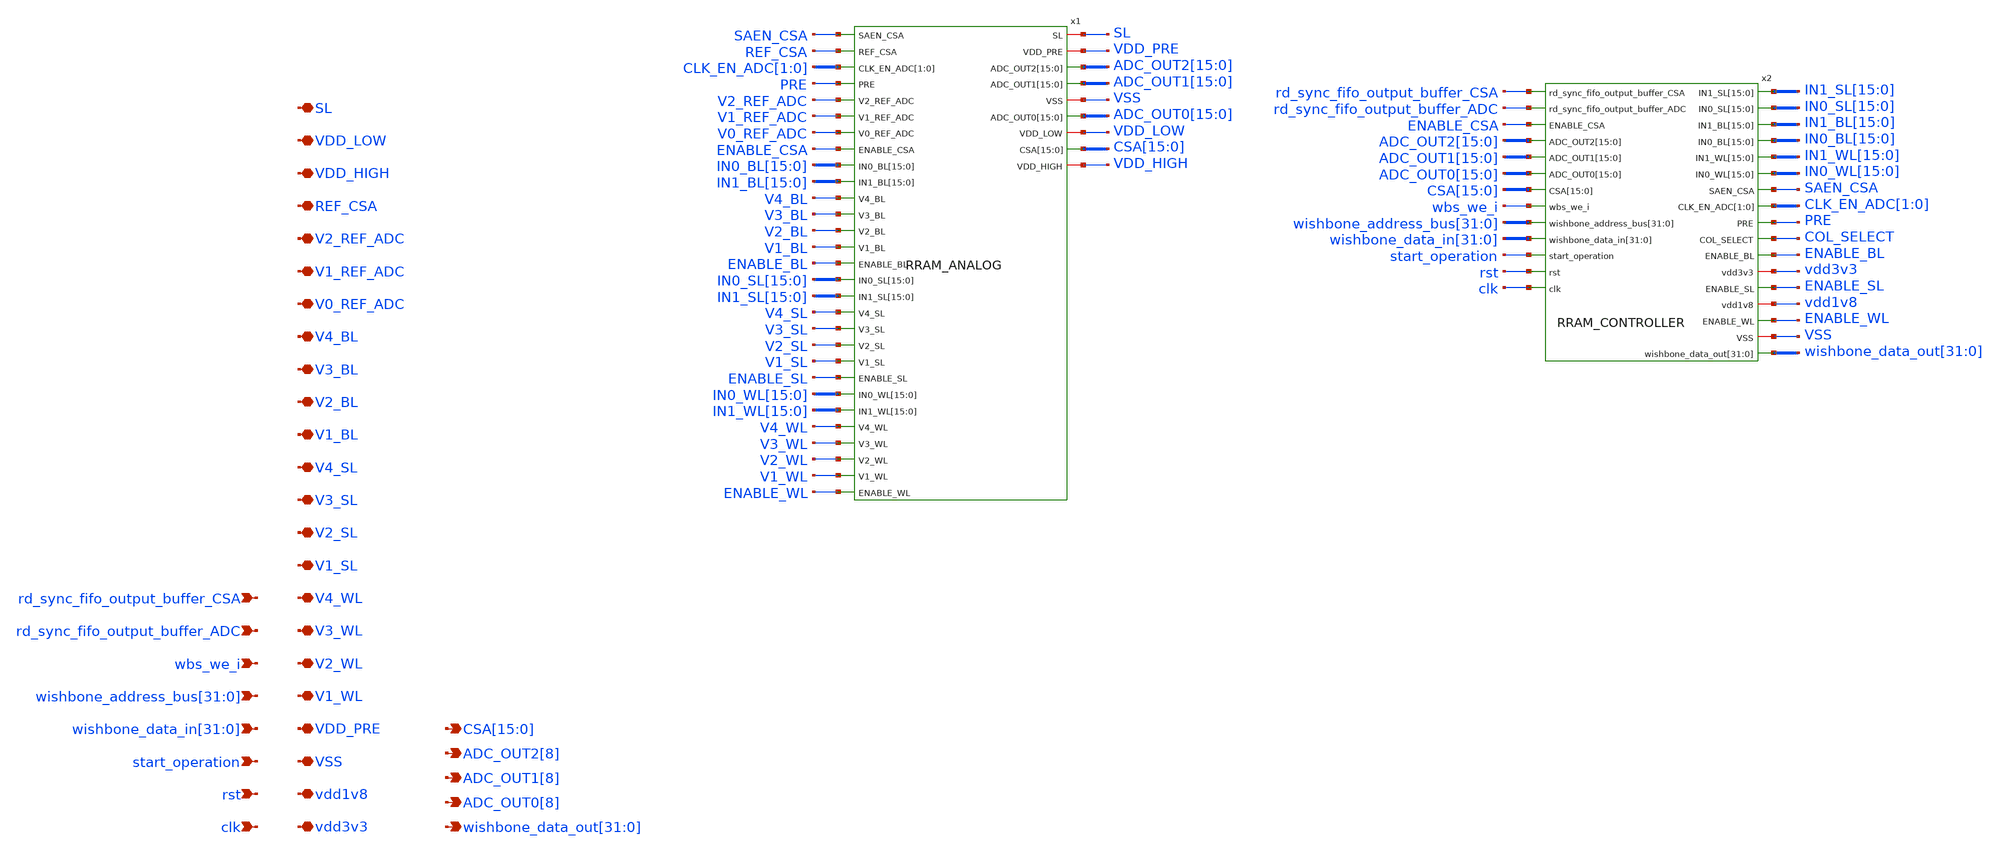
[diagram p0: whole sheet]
** sch_path: xschem/top_wrapper.sch
**.subckt top_wrapper clk rst vdd3v3
*+ wishbone_data_out[31],wishbone_data_out[30],wishbone_data_out[29],wishbone_data_out[28],wishbone_data_out[27],wishbone_data_out[26],wishbone_data_out[25],wishbone_data_out[24],wishbone_data_out[23],wishbone_data_out[22],wishbone_data_out[21],wishbone_data_out[20],wishbone_data_out[19],wishbone_data_out[18],wishbone_data_out[17],wishbone_data_out[16],wishbone_data_out[15],wishbone_data_out[14],wishbone_data_out[13],wishbone_data_out[12],wishbone_data_out[11],wishbone_data_out[10],wishbone_data_out[9],wishbone_data_out[8],wishbone_data_out[7],wishbone_data_out[6],wishbone_data_out[5],wishbone_data_out[4],wishbone_data_out[3],wishbone_data_out[2],wishbone_data_out[1],wishbone_data_out[0] ADC_OUT0[8] vdd1v8 start_operation
*+ wishbone_data_in[31],wishbone_data_in[30],wishbone_data_in[29],wishbone_data_in[28],wishbone_data_in[27],wishbone_data_in[26],wishbone_data_in[25],wishbone_data_in[24],wishbone_data_in[23],wishbone_data_in[22],wishbone_data_in[21],wishbone_data_in[20],wishbone_data_in[19],wishbone_data_in[18],wishbone_data_in[17],wishbone_data_in[16],wishbone_data_in[15],wishbone_data_in[14],wishbone_data_in[13],wishbone_data_in[12],wishbone_data_in[11],wishbone_data_in[10],wishbone_data_in[9],wishbone_data_in[8],wishbone_data_in[7],wishbone_data_in[6],wishbone_data_in[5],wishbone_data_in[4],wishbone_data_in[3],wishbone_data_in[2],wishbone_data_in[1],wishbone_data_in[0]
*+ wishbone_address_bus[31],wishbone_address_bus[30],wishbone_address_bus[29],wishbone_address_bus[28],wishbone_address_bus[27],wishbone_address_bus[26],wishbone_address_bus[25],wishbone_address_bus[24],wishbone_address_bus[23],wishbone_address_bus[22],wishbone_address_bus[21],wishbone_address_bus[20],wishbone_address_bus[19],wishbone_address_bus[18],wishbone_address_bus[17],wishbone_address_bus[16],wishbone_address_bus[15],wishbone_address_bus[14],wishbone_address_bus[13],wishbone_address_bus[12],wishbone_address_bus[11],wishbone_address_bus[10],wishbone_address_bus[9],wishbone_address_bus[8],wishbone_address_bus[7],wishbone_address_bus[6],wishbone_address_bus[5],wishbone_address_bus[4],wishbone_address_bus[3],wishbone_address_bus[2],wishbone_address_bus[1],wishbone_address_bus[0] wbs_we_i VSS VDD_PRE V1_WL V2_WL V3_WL V4_WL V1_SL V2_SL V3_SL V4_SL V1_BL V2_BL V3_BL V4_BL
*+ V0_REF_ADC V1_REF_ADC V2_REF_ADC REF_CSA ADC_OUT1[8] ADC_OUT2[8]
*+ CSA[15],CSA[14],CSA[13],CSA[12],CSA[11],CSA[10],CSA[9],CSA[8],CSA[7],CSA[6],CSA[5],CSA[4],CSA[3],CSA[2],CSA[1],CSA[0] rd_sync_fifo_output_buffer_ADC rd_sync_fifo_output_buffer_CSA VDD_HIGH VDD_LOW SL
*.ipin clk
*.ipin rst
*.iopin vdd3v3
*.opin
*+ wishbone_data_out[31],wishbone_data_out[30],wishbone_data_out[29],wishbone_data_out[28],wishbone_data_out[27],wishbone_data_out[26],wishbone_data_out[25],wishbone_data_out[24],wishbone_data_out[23],wishbone_data_out[22],wishbone_data_out[21],wishbone_data_out[20],wishbone_data_out[19],wishbone_data_out[18],wishbone_data_out[17],wishbone_data_out[16],wishbone_data_out[15],wishbone_data_out[14],wishbone_data_out[13],wishbone_data_out[12],wishbone_data_out[11],wishbone_data_out[10],wishbone_data_out[9],wishbone_data_out[8],wishbone_data_out[7],wishbone_data_out[6],wishbone_data_out[5],wishbone_data_out[4],wishbone_data_out[3],wishbone_data_out[2],wishbone_data_out[1],wishbone_data_out[0]
*.opin ADC_OUT0[8]
*.iopin vdd1v8
*.ipin start_operation
*.ipin
*+ wishbone_data_in[31],wishbone_data_in[30],wishbone_data_in[29],wishbone_data_in[28],wishbone_data_in[27],wishbone_data_in[26],wishbone_data_in[25],wishbone_data_in[24],wishbone_data_in[23],wishbone_data_in[22],wishbone_data_in[21],wishbone_data_in[20],wishbone_data_in[19],wishbone_data_in[18],wishbone_data_in[17],wishbone_data_in[16],wishbone_data_in[15],wishbone_data_in[14],wishbone_data_in[13],wishbone_data_in[12],wishbone_data_in[11],wishbone_data_in[10],wishbone_data_in[9],wishbone_data_in[8],wishbone_data_in[7],wishbone_data_in[6],wishbone_data_in[5],wishbone_data_in[4],wishbone_data_in[3],wishbone_data_in[2],wishbone_data_in[1],wishbone_data_in[0]
*.ipin
*+ wishbone_address_bus[31],wishbone_address_bus[30],wishbone_address_bus[29],wishbone_address_bus[28],wishbone_address_bus[27],wishbone_address_bus[26],wishbone_address_bus[25],wishbone_address_bus[24],wishbone_address_bus[23],wishbone_address_bus[22],wishbone_address_bus[21],wishbone_address_bus[20],wishbone_address_bus[19],wishbone_address_bus[18],wishbone_address_bus[17],wishbone_address_bus[16],wishbone_address_bus[15],wishbone_address_bus[14],wishbone_address_bus[13],wishbone_address_bus[12],wishbone_address_bus[11],wishbone_address_bus[10],wishbone_address_bus[9],wishbone_address_bus[8],wishbone_address_bus[7],wishbone_address_bus[6],wishbone_address_bus[5],wishbone_address_bus[4],wishbone_address_bus[3],wishbone_address_bus[2],wishbone_address_bus[1],wishbone_address_bus[0]
*.ipin wbs_we_i
*.iopin VSS
*.iopin VDD_PRE
*.iopin V1_WL
*.iopin V2_WL
*.iopin V3_WL
*.iopin V4_WL
*.iopin V1_SL
*.iopin V2_SL
*.iopin V3_SL
*.iopin V4_SL
*.iopin V1_BL
*.iopin V2_BL
*.iopin V3_BL
*.iopin V4_BL
*.iopin V0_REF_ADC
*.iopin V1_REF_ADC
*.iopin V2_REF_ADC
*.iopin REF_CSA
*.opin ADC_OUT1[8]
*.opin ADC_OUT2[8]
*.opin
*+ CSA[15],CSA[14],CSA[13],CSA[12],CSA[11],CSA[10],CSA[9],CSA[8],CSA[7],CSA[6],CSA[5],CSA[4],CSA[3],CSA[2],CSA[1],CSA[0]
*.ipin rd_sync_fifo_output_buffer_ADC
*.ipin rd_sync_fifo_output_buffer_CSA
*.iopin VDD_HIGH
*.iopin VDD_LOW
*.iopin SL
x1 SAEN_CSA REF_CSA CLK_EN_ADC[1] CLK_EN_ADC[0] PRE V2_REF_ADC V1_REF_ADC V0_REF_ADC ENABLE_CSA
+ IN0_BL[15] IN0_BL[14] IN0_BL[13] IN0_BL[12] IN0_BL[11] IN0_BL[10] IN0_BL[9] IN0_BL[8] IN0_BL[7] IN0_BL[6]
+ IN0_BL[5] IN0_BL[4] IN0_BL[3] IN0_BL[2] IN0_BL[1] IN0_BL[0] IN1_BL[15] IN1_BL[14] IN1_BL[13] IN1_BL[12]
+ IN1_BL[11] IN1_BL[10] IN1_BL[9] IN1_BL[8] IN1_BL[7] IN1_BL[6] IN1_BL[5] IN1_BL[4] IN1_BL[3] IN1_BL[2]
+ IN1_BL[1] IN1_BL[0] V4_BL V3_BL V2_BL V1_BL ENABLE_BL IN0_SL[15] IN0_SL[14] IN0_SL[13] IN0_SL[12] IN0_SL[11]
+ IN0_SL[10] IN0_SL[9] IN0_SL[8] IN0_SL[7] IN0_SL[6] IN0_SL[5] IN0_SL[4] IN0_SL[3] IN0_SL[2] IN0_SL[1] IN0_SL[0]
+ IN1_SL[15] IN1_SL[14] IN1_SL[13] IN1_SL[12] IN1_SL[11] IN1_SL[10] IN1_SL[9] IN1_SL[8] IN1_SL[7] IN1_SL[6]
+ IN1_SL[5] IN1_SL[4] IN1_SL[3] IN1_SL[2] IN1_SL[1] IN1_SL[0] V4_SL V3_SL V2_SL V1_SL ENABLE_SL IN0_WL[15]
+ IN0_WL[14] IN0_WL[13] IN0_WL[12] IN0_WL[11] IN0_WL[10] IN0_WL[9] IN0_WL[8] IN0_WL[7] IN0_WL[6] IN0_WL[5]
+ IN0_WL[4] IN0_WL[3] IN0_WL[2] IN0_WL[1] IN0_WL[0] IN1_WL[15] IN1_WL[14] IN1_WL[13] IN1_WL[12] IN1_WL[11]
+ IN1_WL[10] IN1_WL[9] IN1_WL[8] IN1_WL[7] IN1_WL[6] IN1_WL[5] IN1_WL[4] IN1_WL[3] IN1_WL[2] IN1_WL[1] IN1_WL[0]
+ V4_WL SL V3_WL VDD_PRE ADC_OUT2[15] ADC_OUT2[14] ADC_OUT2[13] ADC_OUT2[12] ADC_OUT2[11] ADC_OUT2[10]
+ ADC_OUT2[9] ADC_OUT2[8] ADC_OUT2[7] ADC_OUT2[6] ADC_OUT2[5] ADC_OUT2[4] ADC_OUT2[3] ADC_OUT2[2] ADC_OUT2[1]
+ ADC_OUT2[0] V2_WL ADC_OUT1[15] ADC_OUT1[14] ADC_OUT1[13] ADC_OUT1[12] ADC_OUT1[11] ADC_OUT1[10] ADC_OUT1[9]
+ ADC_OUT1[8] ADC_OUT1[7] ADC_OUT1[6] ADC_OUT1[5] ADC_OUT1[4] ADC_OUT1[3] ADC_OUT1[2] ADC_OUT1[1] ADC_OUT1[0] VSS
+ V1_WL ADC_OUT0[15] ADC_OUT0[14] ADC_OUT0[13] ADC_OUT0[12] ADC_OUT0[11] ADC_OUT0[10] ADC_OUT0[9]
+ ADC_OUT0[8] ADC_OUT0[7] ADC_OUT0[6] ADC_OUT0[5] ADC_OUT0[4] ADC_OUT0[3] ADC_OUT0[2] ADC_OUT0[1] ADC_OUT0[0]
+ VDD_LOW CSA[15] CSA[14] CSA[13] CSA[12] CSA[11] CSA[10] CSA[9] CSA[8] CSA[7] CSA[6] CSA[5] CSA[4] CSA[3]
+ CSA[2] CSA[1] CSA[0] ENABLE_WL VDD_HIGH RRAM_ANALOG
x2 rd_sync_fifo_output_buffer_CSA rd_sync_fifo_output_buffer_ADC ENABLE_CSA IN1_SL[15] IN1_SL[14]
+ IN1_SL[13] IN1_SL[12] IN1_SL[11] IN1_SL[10] IN1_SL[9] IN1_SL[8] IN1_SL[7] IN1_SL[6] IN1_SL[5] IN1_SL[4]
+ IN1_SL[3] IN1_SL[2] IN1_SL[1] IN1_SL[0] IN0_SL[15] IN0_SL[14] IN0_SL[13] IN0_SL[12] IN0_SL[11] IN0_SL[10]
+ IN0_SL[9] IN0_SL[8] IN0_SL[7] IN0_SL[6] IN0_SL[5] IN0_SL[4] IN0_SL[3] IN0_SL[2] IN0_SL[1] IN0_SL[0]
+ ADC_OUT2[15] ADC_OUT2[14] ADC_OUT2[13] ADC_OUT2[12] ADC_OUT2[11] ADC_OUT2[10] ADC_OUT2[9] ADC_OUT2[8]
+ ADC_OUT2[7] ADC_OUT2[6] ADC_OUT2[5] ADC_OUT2[4] ADC_OUT2[3] ADC_OUT2[2] ADC_OUT2[1] ADC_OUT2[0] IN1_BL[15]
+ IN1_BL[14] IN1_BL[13] IN1_BL[12] IN1_BL[11] IN1_BL[10] IN1_BL[9] IN1_BL[8] IN1_BL[7] IN1_BL[6] IN1_BL[5]
+ IN1_BL[4] IN1_BL[3] IN1_BL[2] IN1_BL[1] IN1_BL[0] ADC_OUT1[15] ADC_OUT1[14] ADC_OUT1[13] ADC_OUT1[12]
+ ADC_OUT1[11] ADC_OUT1[10] ADC_OUT1[9] ADC_OUT1[8] ADC_OUT1[7] ADC_OUT1[6] ADC_OUT1[5] ADC_OUT1[4] ADC_OUT1[3]
+ ADC_OUT1[2] ADC_OUT1[1] ADC_OUT1[0] IN0_BL[15] IN0_BL[14] IN0_BL[13] IN0_BL[12] IN0_BL[11] IN0_BL[10] IN0_BL[9]
+ IN0_BL[8] IN0_BL[7] IN0_BL[6] IN0_BL[5] IN0_BL[4] IN0_BL[3] IN0_BL[2] IN0_BL[1] IN0_BL[0] ADC_OUT0[15]
+ ADC_OUT0[14] ADC_OUT0[13] ADC_OUT0[12] ADC_OUT0[11] ADC_OUT0[10] ADC_OUT0[9] ADC_OUT0[8] ADC_OUT0[7] ADC_OUT0[6]
+ ADC_OUT0[5] ADC_OUT0[4] ADC_OUT0[3] ADC_OUT0[2] ADC_OUT0[1] ADC_OUT0[0] IN1_WL[15] IN1_WL[14] IN1_WL[13]
+ IN1_WL[12] IN1_WL[11] IN1_WL[10] IN1_WL[9] IN1_WL[8] IN1_WL[7] IN1_WL[6] IN1_WL[5] IN1_WL[4] IN1_WL[3]
+ IN1_WL[2] IN1_WL[1] IN1_WL[0] IN0_WL[15] IN0_WL[14] IN0_WL[13] IN0_WL[12] IN0_WL[11] IN0_WL[10] IN0_WL[9]
+ IN0_WL[8] IN0_WL[7] IN0_WL[6] IN0_WL[5] IN0_WL[4] IN0_WL[3] IN0_WL[2] IN0_WL[1] IN0_WL[0] CSA[15] CSA[14]
+ CSA[13] CSA[12] CSA[11] CSA[10] CSA[9] CSA[8] CSA[7] CSA[6] CSA[5] CSA[4] CSA[3] CSA[2] CSA[1] CSA[0]
+ SAEN_CSA wbs_we_i CLK_EN_ADC[1] CLK_EN_ADC[0] wishbone_address_bus[31] wishbone_address_bus[30]
+ wishbone_address_bus[29] wishbone_address_bus[28] wishbone_address_bus[27] wishbone_address_bus[26] wishbone_address_bus[25]
+ wishbone_address_bus[24] wishbone_address_bus[23] wishbone_address_bus[22] wishbone_address_bus[21] wishbone_address_bus[20]
+ wishbone_address_bus[19] wishbone_address_bus[18] wishbone_address_bus[17] wishbone_address_bus[16] wishbone_address_bus[15]
+ wishbone_address_bus[14] wishbone_address_bus[13] wishbone_address_bus[12] wishbone_address_bus[11] wishbone_address_bus[10]
+ wishbone_address_bus[9] wishbone_address_bus[8] wishbone_address_bus[7] wishbone_address_bus[6] wishbone_address_bus[5]
+ wishbone_address_bus[4] wishbone_address_bus[3] wishbone_address_bus[2] wishbone_address_bus[1] wishbone_address_bus[0] PRE
+ wishbone_data_in[31] wishbone_data_in[30] wishbone_data_in[29] wishbone_data_in[28] wishbone_data_in[27]
+ wishbone_data_in[26] wishbone_data_in[25] wishbone_data_in[24] wishbone_data_in[23] wishbone_data_in[22]
+ wishbone_data_in[21] wishbone_data_in[20] wishbone_data_in[19] wishbone_data_in[18] wishbone_data_in[17]
+ wishbone_data_in[16] wishbone_data_in[15] wishbone_data_in[14] wishbone_data_in[13] wishbone_data_in[12]
+ wishbone_data_in[11] wishbone_data_in[10] wishbone_data_in[9] wishbone_data_in[8] wishbone_data_in[7]
+ wishbone_data_in[6] wishbone_data_in[5] wishbone_data_in[4] wishbone_data_in[3] wishbone_data_in[2] wishbone_data_in[1]
+ wishbone_data_in[0] COL_SELECT ENABLE_BL start_operation vdd3v3 ENABLE_SL vdd1v8 rst ENABLE_WL VSS
+ wishbone_data_out[31] wishbone_data_out[30] wishbone_data_out[29] wishbone_data_out[28] wishbone_data_out[27]
+ wishbone_data_out[26] wishbone_data_out[25] wishbone_data_out[24] wishbone_data_out[23] wishbone_data_out[22]
+ wishbone_data_out[21] wishbone_data_out[20] wishbone_data_out[19] wishbone_data_out[18] wishbone_data_out[17]
+ wishbone_data_out[16] wishbone_data_out[15] wishbone_data_out[14] wishbone_data_out[13] wishbone_data_out[12]
+ wishbone_data_out[11] wishbone_data_out[10] wishbone_data_out[9] wishbone_data_out[8] wishbone_data_out[7]
+ wishbone_data_out[6] wishbone_data_out[5] wishbone_data_out[4] wishbone_data_out[3] wishbone_data_out[2]
+ wishbone_data_out[1] wishbone_data_out[0] clk RRAM_CONTROLLER
**.ends

* expanding   symbol:  RRAM_IMC/xschem/RRAM_ANALOG.sym # of pins=38
** sym_path: xschem/RRAM_ANALOG.sym
** sch_path: xschem/RRAM_ANALOG.sch
.subckt RRAM_ANALOG SAEN_CSA REF_CSA CLK_EN_ADC[1] CLK_EN_ADC[0] PRE V2_REF_ADC V1_REF_ADC
+ V0_REF_ADC ENABLE_CSA IN0_BL[15] IN0_BL[14] IN0_BL[13] IN0_BL[12] IN0_BL[11] IN0_BL[10] IN0_BL[9] IN0_BL[8]
+ IN0_BL[7] IN0_BL[6] IN0_BL[5] IN0_BL[4] IN0_BL[3] IN0_BL[2] IN0_BL[1] IN0_BL[0] IN1_BL[15] IN1_BL[14]
+ IN1_BL[13] IN1_BL[12] IN1_BL[11] IN1_BL[10] IN1_BL[9] IN1_BL[8] IN1_BL[7] IN1_BL[6] IN1_BL[5] IN1_BL[4]
+ IN1_BL[3] IN1_BL[2] IN1_BL[1] IN1_BL[0] V4_BL V3_BL V2_BL V1_BL ENABLE_BL IN0_SL[15] IN0_SL[14] IN0_SL[13]
+ IN0_SL[12] IN0_SL[11] IN0_SL[10] IN0_SL[9] IN0_SL[8] IN0_SL[7] IN0_SL[6] IN0_SL[5] IN0_SL[4] IN0_SL[3]
+ IN0_SL[2] IN0_SL[1] IN0_SL[0] IN1_SL[15] IN1_SL[14] IN1_SL[13] IN1_SL[12] IN1_SL[11] IN1_SL[10] IN1_SL[9]
+ IN1_SL[8] IN1_SL[7] IN1_SL[6] IN1_SL[5] IN1_SL[4] IN1_SL[3] IN1_SL[2] IN1_SL[1] IN1_SL[0] V4_SL V3_SL V2_SL
+ V1_SL ENABLE_SL IN0_WL[15] IN0_WL[14] IN0_WL[13] IN0_WL[12] IN0_WL[11] IN0_WL[10] IN0_WL[9] IN0_WL[8]
+ IN0_WL[7] IN0_WL[6] IN0_WL[5] IN0_WL[4] IN0_WL[3] IN0_WL[2] IN0_WL[1] IN0_WL[0] IN1_WL[15] IN1_WL[14]
+ IN1_WL[13] IN1_WL[12] IN1_WL[11] IN1_WL[10] IN1_WL[9] IN1_WL[8] IN1_WL[7] IN1_WL[6] IN1_WL[5] IN1_WL[4]
+ IN1_WL[3] IN1_WL[2] IN1_WL[1] IN1_WL[0] V4_WL SL V3_WL VDD_PRE ADC_OUT2[15] ADC_OUT2[14] ADC_OUT2[13]
+ ADC_OUT2[12] ADC_OUT2[11] ADC_OUT2[10] ADC_OUT2[9] ADC_OUT2[8] ADC_OUT2[7] ADC_OUT2[6] ADC_OUT2[5] ADC_OUT2[4]
+ ADC_OUT2[3] ADC_OUT2[2] ADC_OUT2[1] ADC_OUT2[0] V2_WL ADC_OUT1[15] ADC_OUT1[14] ADC_OUT1[13] ADC_OUT1[12]
+ ADC_OUT1[11] ADC_OUT1[10] ADC_OUT1[9] ADC_OUT1[8] ADC_OUT1[7] ADC_OUT1[6] ADC_OUT1[5] ADC_OUT1[4] ADC_OUT1[3]
+ ADC_OUT1[2] ADC_OUT1[1] ADC_OUT1[0] VSS V1_WL ADC_OUT0[15] ADC_OUT0[14] ADC_OUT0[13] ADC_OUT0[12] ADC_OUT0[11]
+ ADC_OUT0[10] ADC_OUT0[9] ADC_OUT0[8] ADC_OUT0[7] ADC_OUT0[6] ADC_OUT0[5] ADC_OUT0[4] ADC_OUT0[3] ADC_OUT0[2]
+ ADC_OUT0[1] ADC_OUT0[0] VDD_LOW CSA[15] CSA[14] CSA[13] CSA[12] CSA[11] CSA[10] CSA[9] CSA[8] CSA[7] CSA[6]
+ CSA[5] CSA[4] CSA[3] CSA[2] CSA[1] CSA[0] ENABLE_WL VDD_HIGH
*.iopin VDD_HIGH
*.iopin VDD_LOW
*.opin
*+ CSA[15],CSA[14],CSA[13],CSA[12],CSA[11],CSA[10],CSA[9],CSA[8],CSA[7],CSA[6],CSA[5],CSA[4],CSA[3],CSA[2],CSA[1],CSA[0]
*.ipin V1_WL
*.ipin V2_WL
*.ipin V3_WL
*.ipin V4_WL
*.ipin
*+ IN1_WL[15],IN1_WL[14],IN1_WL[13],IN1_WL[12],IN1_WL[11],IN1_WL[10],IN1_WL[9],IN1_WL[8],IN1_WL[7],IN1_WL[6],IN1_WL[5],IN1_WL[4],IN1_WL[3],IN1_WL[2],IN1_WL[1],IN1_WL[0]
*.ipin
*+ IN0_WL[15],IN0_WL[14],IN0_WL[13],IN0_WL[12],IN0_WL[11],IN0_WL[10],IN0_WL[9],IN0_WL[8],IN0_WL[7],IN0_WL[6],IN0_WL[5],IN0_WL[4],IN0_WL[3],IN0_WL[2],IN0_WL[1],IN0_WL[0]
*.ipin ENABLE_SL
*.ipin V1_SL
*.ipin V2_SL
*.ipin V3_SL
*.ipin V4_SL
*.ipin
*+ IN1_SL[15],IN1_SL[14],IN1_SL[13],IN1_SL[12],IN1_SL[11],IN1_SL[10],IN1_SL[9],IN1_SL[8],IN1_SL[7],IN1_SL[6],IN1_SL[5],IN1_SL[4],IN1_SL[3],IN1_SL[2],IN1_SL[1],IN1_SL[0]
*.ipin
*+ IN0_SL[15],IN0_SL[14],IN0_SL[13],IN0_SL[12],IN0_SL[11],IN0_SL[10],IN0_SL[9],IN0_SL[8],IN0_SL[7],IN0_SL[6],IN0_SL[5],IN0_SL[4],IN0_SL[3],IN0_SL[2],IN0_SL[1],IN0_SL[0]
*.ipin ENABLE_BL
*.ipin V1_BL
*.ipin V2_BL
*.ipin V3_BL
*.ipin V4_BL
*.ipin
*+ IN1_BL[15],IN1_BL[14],IN1_BL[13],IN1_BL[12],IN1_BL[11],IN1_BL[10],IN1_BL[9],IN1_BL[8],IN1_BL[7],IN1_BL[6],IN1_BL[5],IN1_BL[4],IN1_BL[3],IN1_BL[2],IN1_BL[1],IN1_BL[0]
*.ipin
*+ IN0_BL[15],IN0_BL[14],IN0_BL[13],IN0_BL[12],IN0_BL[11],IN0_BL[10],IN0_BL[9],IN0_BL[8],IN0_BL[7],IN0_BL[6],IN0_BL[5],IN0_BL[4],IN0_BL[3],IN0_BL[2],IN0_BL[1],IN0_BL[0]
*.ipin ENABLE_CSA
*.ipin V0_REF_ADC
*.ipin V1_REF_ADC
*.ipin V2_REF_ADC
*.ipin PRE
*.iopin VSS
*.opin
*+ ADC_OUT0[15],ADC_OUT0[14],ADC_OUT0[13],ADC_OUT0[12],ADC_OUT0[11],ADC_OUT0[10],ADC_OUT0[9],ADC_OUT0[8],ADC_OUT0[7],ADC_OUT0[6],ADC_OUT0[5],ADC_OUT0[4],ADC_OUT0[3],ADC_OUT0[2],ADC_OUT0[1],ADC_OUT0[0]
*.opin
*+ ADC_OUT1[15],ADC_OUT1[14],ADC_OUT1[13],ADC_OUT1[12],ADC_OUT1[11],ADC_OUT1[10],ADC_OUT1[9],ADC_OUT1[8],ADC_OUT1[7],ADC_OUT1[6],ADC_OUT1[5],ADC_OUT1[4],ADC_OUT1[3],ADC_OUT1[2],ADC_OUT1[1],ADC_OUT1[0]
*.opin
*+ ADC_OUT2[15],ADC_OUT2[14],ADC_OUT2[13],ADC_OUT2[12],ADC_OUT2[11],ADC_OUT2[10],ADC_OUT2[9],ADC_OUT2[8],ADC_OUT2[7],ADC_OUT2[6],ADC_OUT2[5],ADC_OUT2[4],ADC_OUT2[3],ADC_OUT2[2],ADC_OUT2[1],ADC_OUT2[0]
*.ipin CLK_EN_ADC[1],CLK_EN_ADC[0]
*.ipin REF_CSA
*.ipin SAEN_CSA
*.ipin ENABLE_WL
*.iopin VDD_PRE
*.iopin SL
.ends


* expanding   symbol:  RRAM_IMC/xschem/RRAM_CONTROLLER.sym # of pins=30
** sym_path: xschem/RRAM_CONTROLLER.sym
** sch_path: xschem/RRAM_CONTROLLER.sch
.subckt RRAM_CONTROLLER rd_sync_fifo_output_buffer_CSA rd_sync_fifo_output_buffer_ADC ENABLE_CSA
+ IN1_SL[15] IN1_SL[14] IN1_SL[13] IN1_SL[12] IN1_SL[11] IN1_SL[10] IN1_SL[9] IN1_SL[8] IN1_SL[7] IN1_SL[6]
+ IN1_SL[5] IN1_SL[4] IN1_SL[3] IN1_SL[2] IN1_SL[1] IN1_SL[0] IN0_SL[15] IN0_SL[14] IN0_SL[13] IN0_SL[12]
+ IN0_SL[11] IN0_SL[10] IN0_SL[9] IN0_SL[8] IN0_SL[7] IN0_SL[6] IN0_SL[5] IN0_SL[4] IN0_SL[3] IN0_SL[2]
+ IN0_SL[1] IN0_SL[0] ADC_OUT2[15] ADC_OUT2[14] ADC_OUT2[13] ADC_OUT2[12] ADC_OUT2[11] ADC_OUT2[10] ADC_OUT2[9]
+ ADC_OUT2[8] ADC_OUT2[7] ADC_OUT2[6] ADC_OUT2[5] ADC_OUT2[4] ADC_OUT2[3] ADC_OUT2[2] ADC_OUT2[1] ADC_OUT2[0]
+ IN1_BL[15] IN1_BL[14] IN1_BL[13] IN1_BL[12] IN1_BL[11] IN1_BL[10] IN1_BL[9] IN1_BL[8] IN1_BL[7] IN1_BL[6]
+ IN1_BL[5] IN1_BL[4] IN1_BL[3] IN1_BL[2] IN1_BL[1] IN1_BL[0] ADC_OUT1[15] ADC_OUT1[14] ADC_OUT1[13]
+ ADC_OUT1[12] ADC_OUT1[11] ADC_OUT1[10] ADC_OUT1[9] ADC_OUT1[8] ADC_OUT1[7] ADC_OUT1[6] ADC_OUT1[5] ADC_OUT1[4]
+ ADC_OUT1[3] ADC_OUT1[2] ADC_OUT1[1] ADC_OUT1[0] IN0_BL[15] IN0_BL[14] IN0_BL[13] IN0_BL[12] IN0_BL[11]
+ IN0_BL[10] IN0_BL[9] IN0_BL[8] IN0_BL[7] IN0_BL[6] IN0_BL[5] IN0_BL[4] IN0_BL[3] IN0_BL[2] IN0_BL[1] IN0_BL[0]
+ ADC_OUT0[15] ADC_OUT0[14] ADC_OUT0[13] ADC_OUT0[12] ADC_OUT0[11] ADC_OUT0[10] ADC_OUT0[9] ADC_OUT0[8]
+ ADC_OUT0[7] ADC_OUT0[6] ADC_OUT0[5] ADC_OUT0[4] ADC_OUT0[3] ADC_OUT0[2] ADC_OUT0[1] ADC_OUT0[0] IN1_WL[15]
+ IN1_WL[14] IN1_WL[13] IN1_WL[12] IN1_WL[11] IN1_WL[10] IN1_WL[9] IN1_WL[8] IN1_WL[7] IN1_WL[6] IN1_WL[5]
+ IN1_WL[4] IN1_WL[3] IN1_WL[2] IN1_WL[1] IN1_WL[0] IN0_WL[15] IN0_WL[14] IN0_WL[13] IN0_WL[12] IN0_WL[11]
+ IN0_WL[10] IN0_WL[9] IN0_WL[8] IN0_WL[7] IN0_WL[6] IN0_WL[5] IN0_WL[4] IN0_WL[3] IN0_WL[2] IN0_WL[1] IN0_WL[0]
+ CSA[15] CSA[14] CSA[13] CSA[12] CSA[11] CSA[10] CSA[9] CSA[8] CSA[7] CSA[6] CSA[5] CSA[4] CSA[3] CSA[2]
+ CSA[1] CSA[0] SAEN_CSA wbs_we_i CLK_EN_ADC[1] CLK_EN_ADC[0] wishbone_address_bus[31]
+ wishbone_address_bus[30] wishbone_address_bus[29] wishbone_address_bus[28] wishbone_address_bus[27] wishbone_address_bus[26]
+ wishbone_address_bus[25] wishbone_address_bus[24] wishbone_address_bus[23] wishbone_address_bus[22] wishbone_address_bus[21]
+ wishbone_address_bus[20] wishbone_address_bus[19] wishbone_address_bus[18] wishbone_address_bus[17] wishbone_address_bus[16]
+ wishbone_address_bus[15] wishbone_address_bus[14] wishbone_address_bus[13] wishbone_address_bus[12] wishbone_address_bus[11]
+ wishbone_address_bus[10] wishbone_address_bus[9] wishbone_address_bus[8] wishbone_address_bus[7] wishbone_address_bus[6]
+ wishbone_address_bus[5] wishbone_address_bus[4] wishbone_address_bus[3] wishbone_address_bus[2] wishbone_address_bus[1]
+ wishbone_address_bus[0] PRE wishbone_data_in[31] wishbone_data_in[30] wishbone_data_in[29] wishbone_data_in[28]
+ wishbone_data_in[27] wishbone_data_in[26] wishbone_data_in[25] wishbone_data_in[24] wishbone_data_in[23]
+ wishbone_data_in[22] wishbone_data_in[21] wishbone_data_in[20] wishbone_data_in[19] wishbone_data_in[18]
+ wishbone_data_in[17] wishbone_data_in[16] wishbone_data_in[15] wishbone_data_in[14] wishbone_data_in[13]
+ wishbone_data_in[12] wishbone_data_in[11] wishbone_data_in[10] wishbone_data_in[9] wishbone_data_in[8]
+ wishbone_data_in[7] wishbone_data_in[6] wishbone_data_in[5] wishbone_data_in[4] wishbone_data_in[3] wishbone_data_in[2]
+ wishbone_data_in[1] wishbone_data_in[0] COL_SELECT ENABLE_BL start_operation vdd3v3 ENABLE_SL vdd1v8 rst ENABLE_WL VSS
+ wishbone_data_out[31] wishbone_data_out[30] wishbone_data_out[29] wishbone_data_out[28] wishbone_data_out[27]
+ wishbone_data_out[26] wishbone_data_out[25] wishbone_data_out[24] wishbone_data_out[23] wishbone_data_out[22]
+ wishbone_data_out[21] wishbone_data_out[20] wishbone_data_out[19] wishbone_data_out[18] wishbone_data_out[17]
+ wishbone_data_out[16] wishbone_data_out[15] wishbone_data_out[14] wishbone_data_out[13] wishbone_data_out[12]
+ wishbone_data_out[11] wishbone_data_out[10] wishbone_data_out[9] wishbone_data_out[8] wishbone_data_out[7]
+ wishbone_data_out[6] wishbone_data_out[5] wishbone_data_out[4] wishbone_data_out[3] wishbone_data_out[2]
+ wishbone_data_out[1] wishbone_data_out[0] clk
*.ipin clk
*.ipin rst
*.iopin VSS
*.opin
*+ wishbone_data_out[31],wishbone_data_out[30],wishbone_data_out[29],wishbone_data_out[28],wishbone_data_out[27],wishbone_data_out[26],wishbone_data_out[25],wishbone_data_out[24],wishbone_data_out[23],wishbone_data_out[22],wishbone_data_out[21],wishbone_data_out[20],wishbone_data_out[19],wishbone_data_out[18],wishbone_data_out[17],wishbone_data_out[16],wishbone_data_out[15],wishbone_data_out[14],wishbone_data_out[13],wishbone_data_out[12],wishbone_data_out[11],wishbone_data_out[10],wishbone_data_out[9],wishbone_data_out[8],wishbone_data_out[7],wishbone_data_out[6],wishbone_data_out[5],wishbone_data_out[4],wishbone_data_out[3],wishbone_data_out[2],wishbone_data_out[1],wishbone_data_out[0]
*.opin ENABLE_WL
*.ipin start_operation
*.ipin
*+ wishbone_data_in[31],wishbone_data_in[30],wishbone_data_in[29],wishbone_data_in[28],wishbone_data_in[27],wishbone_data_in[26],wishbone_data_in[25],wishbone_data_in[24],wishbone_data_in[23],wishbone_data_in[22],wishbone_data_in[21],wishbone_data_in[20],wishbone_data_in[19],wishbone_data_in[18],wishbone_data_in[17],wishbone_data_in[16],wishbone_data_in[15],wishbone_data_in[14],wishbone_data_in[13],wishbone_data_in[12],wishbone_data_in[11],wishbone_data_in[10],wishbone_data_in[9],wishbone_data_in[8],wishbone_data_in[7],wishbone_data_in[6],wishbone_data_in[5],wishbone_data_in[4],wishbone_data_in[3],wishbone_data_in[2],wishbone_data_in[1],wishbone_data_in[0]
*.ipin
*+ wishbone_address_bus[31],wishbone_address_bus[30],wishbone_address_bus[29],wishbone_address_bus[28],wishbone_address_bus[27],wishbone_address_bus[26],wishbone_address_bus[25],wishbone_address_bus[24],wishbone_address_bus[23],wishbone_address_bus[22],wishbone_address_bus[21],wishbone_address_bus[20],wishbone_address_bus[19],wishbone_address_bus[18],wishbone_address_bus[17],wishbone_address_bus[16],wishbone_address_bus[15],wishbone_address_bus[14],wishbone_address_bus[13],wishbone_address_bus[12],wishbone_address_bus[11],wishbone_address_bus[10],wishbone_address_bus[9],wishbone_address_bus[8],wishbone_address_bus[7],wishbone_address_bus[6],wishbone_address_bus[5],wishbone_address_bus[4],wishbone_address_bus[3],wishbone_address_bus[2],wishbone_address_bus[1],wishbone_address_bus[0]
*.ipin wbs_we_i
*.ipin
*+ CSA[15],CSA[14],CSA[13],CSA[12],CSA[11],CSA[10],CSA[9],CSA[8],CSA[7],CSA[6],CSA[5],CSA[4],CSA[3],CSA[2],CSA[1],CSA[0]
*.ipin
*+ ADC_OUT0[15],ADC_OUT0[14],ADC_OUT0[13],ADC_OUT0[12],ADC_OUT0[11],ADC_OUT0[10],ADC_OUT0[9],ADC_OUT0[8],ADC_OUT0[7],ADC_OUT0[6],ADC_OUT0[5],ADC_OUT0[4],ADC_OUT0[3],ADC_OUT0[2],ADC_OUT0[1],ADC_OUT0[0]
*.ipin
*+ ADC_OUT1[15],ADC_OUT1[14],ADC_OUT1[13],ADC_OUT1[12],ADC_OUT1[11],ADC_OUT1[10],ADC_OUT1[9],ADC_OUT1[8],ADC_OUT1[7],ADC_OUT1[6],ADC_OUT1[5],ADC_OUT1[4],ADC_OUT1[3],ADC_OUT1[2],ADC_OUT1[1],ADC_OUT1[0]
*.ipin
*+ ADC_OUT2[15],ADC_OUT2[14],ADC_OUT2[13],ADC_OUT2[12],ADC_OUT2[11],ADC_OUT2[10],ADC_OUT2[9],ADC_OUT2[8],ADC_OUT2[7],ADC_OUT2[6],ADC_OUT2[5],ADC_OUT2[4],ADC_OUT2[3],ADC_OUT2[2],ADC_OUT2[1],ADC_OUT2[0]
*.ipin ENABLE_CSA
*.ipin rd_sync_fifo_output_buffer_ADC
*.ipin rd_sync_fifo_output_buffer_CSA
*.iopin vdd1v8
*.iopin vdd3v3
*.opin ENABLE_SL
*.opin ENABLE_BL
*.opin COL_SELECT
*.opin PRE
*.opin CLK_EN_ADC[1],CLK_EN_ADC[0]
*.opin SAEN_CSA
*.opin
*+ IN0_WL[15],IN0_WL[14],IN0_WL[13],IN0_WL[12],IN0_WL[11],IN0_WL[10],IN0_WL[9],IN0_WL[8],IN0_WL[7],IN0_WL[6],IN0_WL[5],IN0_WL[4],IN0_WL[3],IN0_WL[2],IN0_WL[1],IN0_WL[0]
*.opin
*+ IN1_WL[15],IN1_WL[14],IN1_WL[13],IN1_WL[12],IN1_WL[11],IN1_WL[10],IN1_WL[9],IN1_WL[8],IN1_WL[7],IN1_WL[6],IN1_WL[5],IN1_WL[4],IN1_WL[3],IN1_WL[2],IN1_WL[1],IN1_WL[0]
*.opin
*+ IN0_BL[15],IN0_BL[14],IN0_BL[13],IN0_BL[12],IN0_BL[11],IN0_BL[10],IN0_BL[9],IN0_BL[8],IN0_BL[7],IN0_BL[6],IN0_BL[5],IN0_BL[4],IN0_BL[3],IN0_BL[2],IN0_BL[1],IN0_BL[0]
*.opin
*+ IN1_BL[15],IN1_BL[14],IN1_BL[13],IN1_BL[12],IN1_BL[11],IN1_BL[10],IN1_BL[9],IN1_BL[8],IN1_BL[7],IN1_BL[6],IN1_BL[5],IN1_BL[4],IN1_BL[3],IN1_BL[2],IN1_BL[1],IN1_BL[0]
*.opin
*+ IN0_SL[15],IN0_SL[14],IN0_SL[13],IN0_SL[12],IN0_SL[11],IN0_SL[10],IN0_SL[9],IN0_SL[8],IN0_SL[7],IN0_SL[6],IN0_SL[5],IN0_SL[4],IN0_SL[3],IN0_SL[2],IN0_SL[1],IN0_SL[0]
*.opin
*+ IN1_SL[15],IN1_SL[14],IN1_SL[13],IN1_SL[12],IN1_SL[11],IN1_SL[10],IN1_SL[9],IN1_SL[8],IN1_SL[7],IN1_SL[6],IN1_SL[5],IN1_SL[4],IN1_SL[3],IN1_SL[2],IN1_SL[1],IN1_SL[0]
.ends

.end
